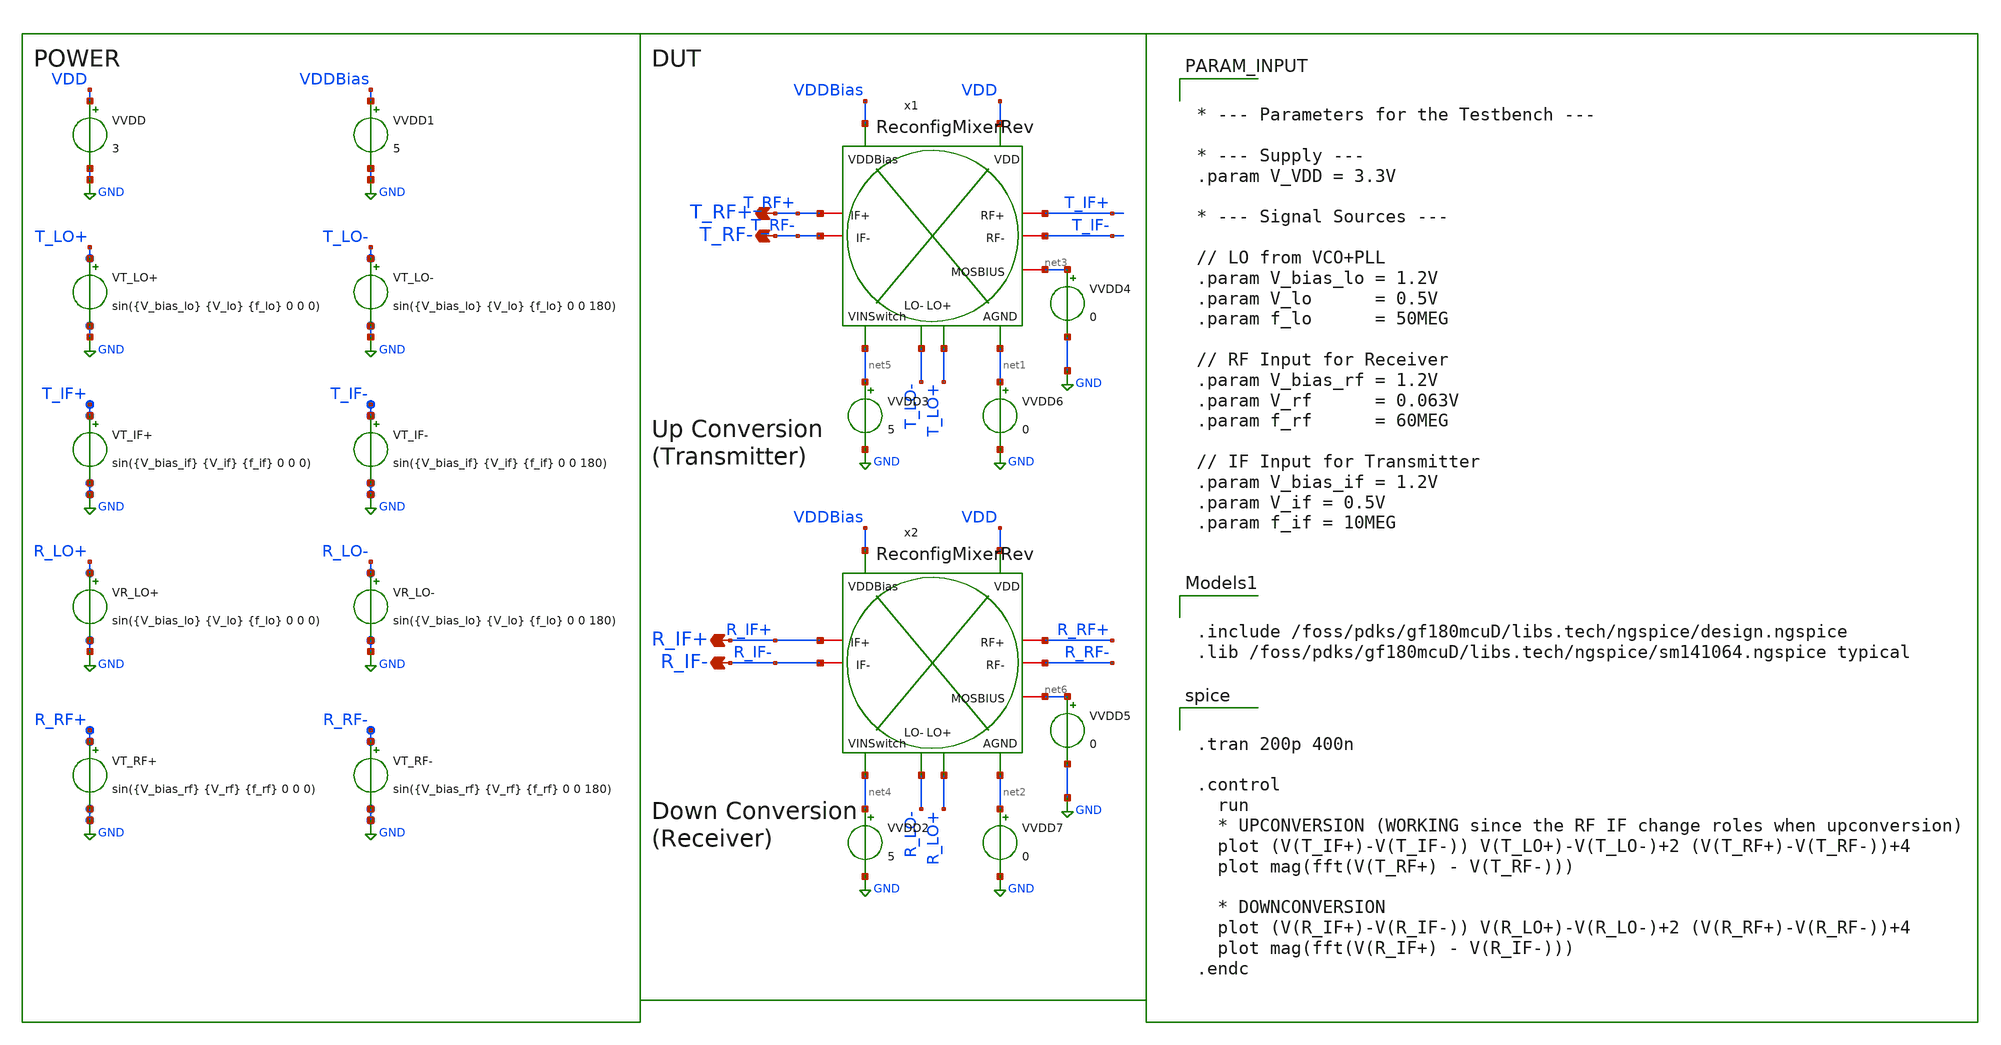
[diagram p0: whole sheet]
** sch_path: Project/1-on-chip/schematic/Mixer/tb_ReconfigMixer.sch
**.subckt tb_ReconfigMixer T_RF+ T_RF- R_IF+ R_IF-
*.opin T_RF+
*.opin T_RF-
*.opin R_IF+
*.opin R_IF-
VVDD VDD GND 3
VT_LO+ T_LO+ GND sin({V_bias_lo} {V_lo} {f_lo} 0 0 0)
VT_LO- T_LO- GND sin({V_bias_lo} {V_lo} {f_lo} 0 0 180)
VT_IF+ T_IF+ GND sin({V_bias_if} {V_if} {f_if} 0 0 0)
VT_IF- T_IF- GND sin({V_bias_if} {V_if} {f_if} 0 0 180)
VR_LO+ R_LO+ GND sin({V_bias_lo} {V_lo} {f_lo} 0 0 0)
VR_LO- R_LO- GND sin({V_bias_lo} {V_lo} {f_lo} 0 0 180)
VT_RF+ R_RF+ GND sin({V_bias_rf} {V_rf} {f_rf} 0 0 0)
VT_RF- R_RF- GND sin({V_bias_rf} {V_rf} {f_rf} 0 0 180)
VVDD1 VDDBias GND 5
x2 VDD R_IF+ R_IF- R_LO+ R_LO- R_RF+ R_RF- net6 VDDBias net2 net4 ReconfigMixerRev
VVDD2 net4 GND 5
VVDD3 net5 GND 5
x1 VDD T_RF+ T_RF- T_LO+ T_LO- T_IF+ T_IF- net3 VDDBias net1 net5 ReconfigMixerRev
VVDD4 net3 GND 0
VVDD5 net6 GND 0
VVDD6 net1 GND 0
VVDD7 net2 GND 0
**** begin user architecture code

.include /foss/pdks/gf180mcuD/libs.tech/ngspice/design.ngspice
.lib /foss/pdks/gf180mcuD/libs.tech/ngspice/sm141064.ngspice typical



* --- Parameters for the Testbench ---

* --- Supply ---
.param V_VDD = 3.3V

* --- Signal Sources ---

// LO from VCO+PLL
.param V_bias_lo = 1.2V
.param V_lo      = 0.5V
.param f_lo      = 50MEG

// RF Input for Receiver
.param V_bias_rf = 1.2V
.param V_rf      = 0.063V
.param f_rf      = 60MEG

// IF Input for Transmitter
.param V_bias_if = 1.2V
.param V_if = 0.5V
.param f_if = 10MEG





.tran 200p 400n

.control
  run
  * UPCONVERSION (WORKING since the RF IF change roles when upconversion)
  plot (V(T_IF+)-V(T_IF-)) V(T_LO+)-V(T_LO-)+2 (V(T_RF+)-V(T_RF-))+4
  plot mag(fft(V(T_RF+) - V(T_RF-)))

  * DOWNCONVERSION
  plot (V(R_IF+)-V(R_IF-)) V(R_LO+)-V(R_LO-)+2 (V(R_RF+)-V(R_RF-))+4
  plot mag(fft(V(R_IF+) - V(R_IF-)))
.endc


**** end user architecture code
**.ends
.GLOBAL GND
.end
